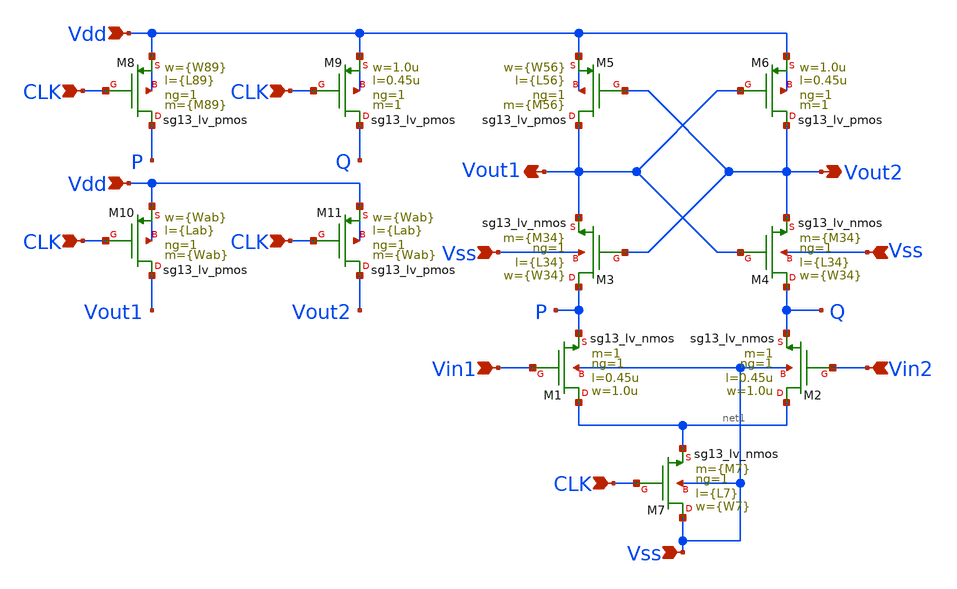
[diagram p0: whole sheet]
** sch_path: xschem/sch/strongarm.sch
**.subckt strongarm Vdd Vss Vout2 Vout1 Vin1 Vin2 Vss Vss CLK CLK CLK Vdd CLK CLK
*.ipin Vdd
*.ipin Vss
*.opin Vout2
*.opin Vout1
*.ipin Vin1
*.ipin Vin2
*.ipin Vss
*.ipin Vss
*.ipin CLK
*.ipin CLK
*.ipin CLK
*.ipin Vdd
*.ipin CLK
*.ipin CLK
XM1 net1 Vin1 P Vss sg13_lv_nmos w=1.0u l=0.45u ng=1 m=1 mm_ok=1
XM2 net1 Vin2 Q Vss sg13_lv_nmos w=1.0u l=0.45u ng=1 m=1 mm_ok=1
XM3 P Vout2 Vout1 Vss sg13_lv_nmos w={W34} l={L34} ng=1 m={M34} mm_ok=1
XM4 Q Vout1 Vout2 Vss sg13_lv_nmos w={W34} l={L34} ng=1 m={M34} mm_ok=1
XM6 Vout2 Vout1 Vdd Vdd sg13_lv_pmos w=1.0u l=0.45u ng=1 m=1 mm_ok=1
XM5 Vout1 Vout2 Vdd Vdd sg13_lv_pmos w={W56} l={L56} ng=1 m={M56} mm_ok=1
XM7 Vss CLK net1 Vss sg13_lv_nmos w={W7} l={L7} ng=1 m={M7} mm_ok=1
XM8 P CLK Vdd Vdd sg13_lv_pmos w={W89} l={L89} ng=1 m={M89} mm_ok=1
XM9 Q CLK Vdd Vdd sg13_lv_pmos w=1.0u l=0.45u ng=1 m=1 mm_ok=1
XM11 Vout2 CLK Vdd Vdd sg13_lv_pmos w={Wab} l={Lab} ng=1 m={Wab} mm_ok=1
XM10 Vout1 CLK Vdd Vdd sg13_lv_pmos w={Wab} l={Lab} ng=1 m={Wab} mm_ok=1
**.ends
.end
